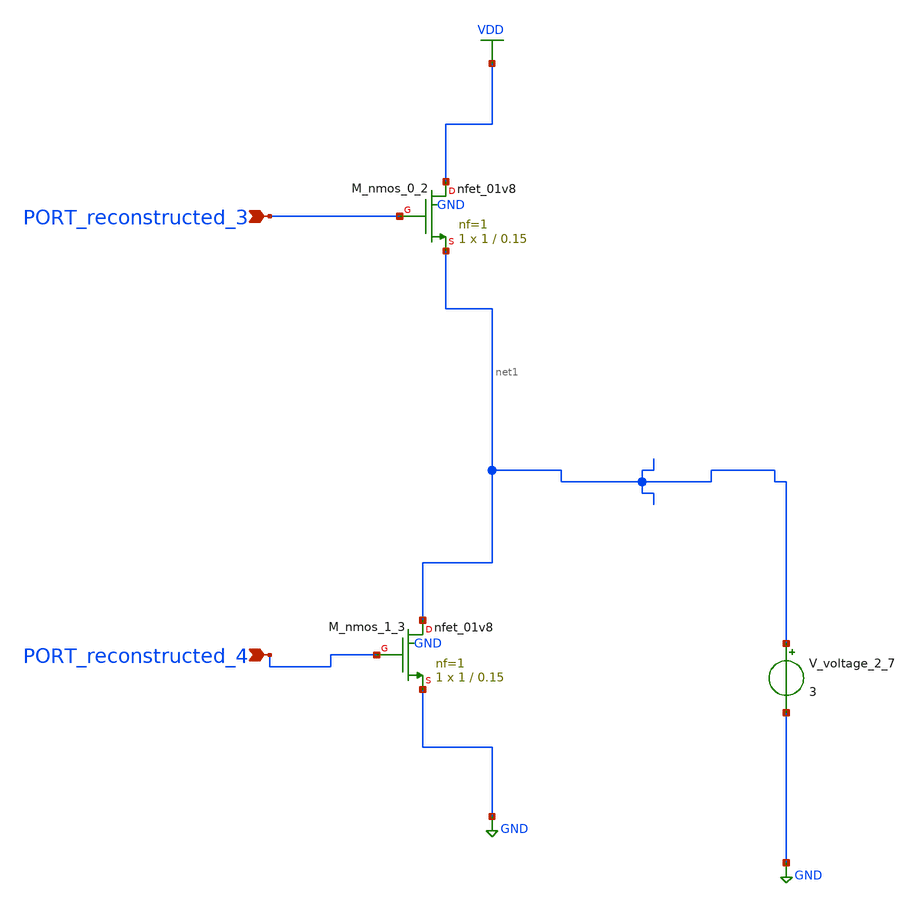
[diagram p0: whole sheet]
** sch_path: schematics/AMSNet/162.sch
**.subckt 162 PORT_reconstructed_4 PORT_reconstructed_3
*.ipin PORT_reconstructed_4
*.ipin PORT_reconstructed_3
XM_nmos_0_2 VDD PORT_reconstructed_3 net1 GND sky130_fd_pr__nfet_01v8 L=0.15 W=1 nf=1 ad='int((1 + 1)/2) * 1 / 1 * 0.29'
+ as='int((1 + 2)/2) * 1 / 1 * 0.29' pd='2*int((1 + 1)/2) * (1 / 1 + 0.29)' ps='2*int((1 + 2)/2) * (1 / 1 + 0.29)'
+ nrd='0.29 / 1 ' nrs='0.29 / 1 ' sa=0 sb=0 sd=0 mult=1 m=1
XM_nmos_1_3 net1 PORT_reconstructed_4 GND GND sky130_fd_pr__nfet_01v8 L=0.15 W=1 nf=1 ad='int((1 + 1)/2) * 1 / 1 * 0.29'
+ as='int((1 + 2)/2) * 1 / 1 * 0.29' pd='2*int((1 + 1)/2) * (1 / 1 + 0.29)' ps='2*int((1 + 2)/2) * (1 / 1 + 0.29)'
+ nrd='0.29 / 1 ' nrs='0.29 / 1 ' sa=0 sb=0 sd=0 mult=1 m=1
V_voltage_2_7 net1 GND 3
**.ends
.GLOBAL GND
.GLOBAL VDD
.end
